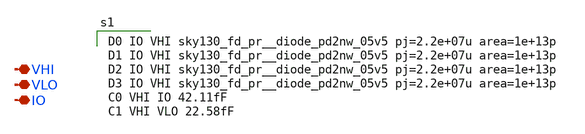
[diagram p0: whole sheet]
** sch_path: xschem/ESD_diode_P_PEX.sch
**.subckt ESD_diode_P_PEX VHI VLO IO
*.iopin VHI
*.iopin VLO
*.iopin IO
**** begin user architecture code

D0 IO VHI sky130_fd_pr__diode_pd2nw_05v5 pj=2.2e+07u area=1e+13p
D1 IO VHI sky130_fd_pr__diode_pd2nw_05v5 pj=2.2e+07u area=1e+13p
D2 IO VHI sky130_fd_pr__diode_pd2nw_05v5 pj=2.2e+07u area=1e+13p
D3 IO VHI sky130_fd_pr__diode_pd2nw_05v5 pj=2.2e+07u area=1e+13p
C0 VHI IO 42.11fF
C1 VHI VLO 22.58fF


**** end user architecture code
**.ends
.end
